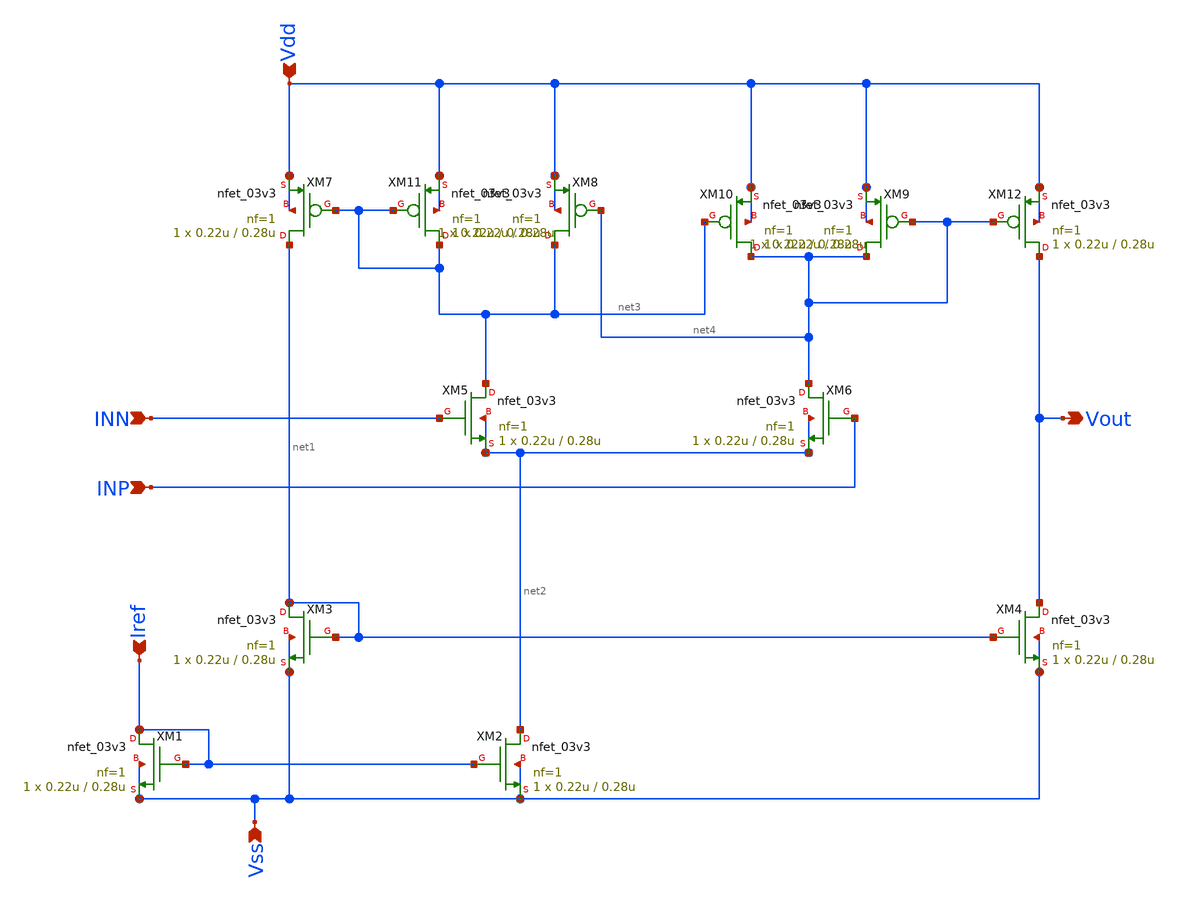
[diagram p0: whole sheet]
** sch_path: designs/libs/core_analog/Comparator/Comparator.sch
**.subckt Comparator Vss Vdd Iref INN INP Vout
*.ipin Vss
*.ipin Vdd
*.ipin Iref
*.ipin INN
*.ipin INP
*.opin Vout
XM1 Iref Iref Vss Vss nfet_03v3 L=0.28u W=0.22u nf=1 ad='int((nf+1)/2) * W/nf * 0.18u' as='int((nf+2)/2) * W/nf * 0.18u'
+ pd='2*int((nf+1)/2) * (W/nf + 0.18u)' ps='2*int((nf+2)/2) * (W/nf + 0.18u)' nrd='0.18u / W' nrs='0.18u / W'
+ sa=0 sb=0 sd=0 m=1
XM2 net2 Iref Vss Vss nfet_03v3 L=0.28u W=0.22u nf=1 ad='int((nf+1)/2) * W/nf * 0.18u' as='int((nf+2)/2) * W/nf * 0.18u'
+ pd='2*int((nf+1)/2) * (W/nf + 0.18u)' ps='2*int((nf+2)/2) * (W/nf + 0.18u)' nrd='0.18u / W' nrs='0.18u / W'
+ sa=0 sb=0 sd=0 m=1
XM3 net1 net1 Vss Vss nfet_03v3 L=0.28u W=0.22u nf=1 ad='int((nf+1)/2) * W/nf * 0.18u' as='int((nf+2)/2) * W/nf * 0.18u'
+ pd='2*int((nf+1)/2) * (W/nf + 0.18u)' ps='2*int((nf+2)/2) * (W/nf + 0.18u)' nrd='0.18u / W' nrs='0.18u / W'
+ sa=0 sb=0 sd=0 m=1
XM4 Vout net1 Vss Vss nfet_03v3 L=0.28u W=0.22u nf=1 ad='int((nf+1)/2) * W/nf * 0.18u' as='int((nf+2)/2) * W/nf * 0.18u'
+ pd='2*int((nf+1)/2) * (W/nf + 0.18u)' ps='2*int((nf+2)/2) * (W/nf + 0.18u)' nrd='0.18u / W' nrs='0.18u / W'
+ sa=0 sb=0 sd=0 m=1
XM5 net3 INN net2 net2 nfet_03v3 L=0.28u W=0.22u nf=1 ad='int((nf+1)/2) * W/nf * 0.18u' as='int((nf+2)/2) * W/nf * 0.18u'
+ pd='2*int((nf+1)/2) * (W/nf + 0.18u)' ps='2*int((nf+2)/2) * (W/nf + 0.18u)' nrd='0.18u / W' nrs='0.18u / W'
+ sa=0 sb=0 sd=0 m=1
XM6 net4 INP net2 net2 nfet_03v3 L=0.28u W=0.22u nf=1 ad='int((nf+1)/2) * W/nf * 0.18u' as='int((nf+2)/2) * W/nf * 0.18u'
+ pd='2*int((nf+1)/2) * (W/nf + 0.18u)' ps='2*int((nf+2)/2) * (W/nf + 0.18u)' nrd='0.18u / W' nrs='0.18u / W'
+ sa=0 sb=0 sd=0 m=1
XM7 net1 net3 Vdd Vdd nfet_03v3 L=0.28u W=0.22u nf=1 ad='int((nf+1)/2) * W/nf * 0.18u' as='int((nf+2)/2) * W/nf * 0.18u'
+ pd='2*int((nf+1)/2) * (W/nf + 0.18u)' ps='2*int((nf+2)/2) * (W/nf + 0.18u)' nrd='0.18u / W' nrs='0.18u / W'
+ sa=0 sb=0 sd=0 m=1
XM8 net3 net4 Vdd Vdd nfet_03v3 L=0.28u W=0.22u nf=1 ad='int((nf+1)/2) * W/nf * 0.18u' as='int((nf+2)/2) * W/nf * 0.18u'
+ pd='2*int((nf+1)/2) * (W/nf + 0.18u)' ps='2*int((nf+2)/2) * (W/nf + 0.18u)' nrd='0.18u / W' nrs='0.18u / W'
+ sa=0 sb=0 sd=0 m=1
XM9 net4 net4 Vdd Vdd nfet_03v3 L=0.28u W=0.22u nf=1 ad='int((nf+1)/2) * W/nf * 0.18u' as='int((nf+2)/2) * W/nf * 0.18u'
+ pd='2*int((nf+1)/2) * (W/nf + 0.18u)' ps='2*int((nf+2)/2) * (W/nf + 0.18u)' nrd='0.18u / W' nrs='0.18u / W'
+ sa=0 sb=0 sd=0 m=1
XM10 net4 net3 Vdd Vdd nfet_03v3 L=0.28u W=0.22u nf=1 ad='int((nf+1)/2) * W/nf * 0.18u' as='int((nf+2)/2) * W/nf * 0.18u'
+ pd='2*int((nf+1)/2) * (W/nf + 0.18u)' ps='2*int((nf+2)/2) * (W/nf + 0.18u)' nrd='0.18u / W' nrs='0.18u / W'
+ sa=0 sb=0 sd=0 m=1
XM11 net3 net3 Vdd Vdd nfet_03v3 L=0.28u W=0.22u nf=1 ad='int((nf+1)/2) * W/nf * 0.18u' as='int((nf+2)/2) * W/nf * 0.18u'
+ pd='2*int((nf+1)/2) * (W/nf + 0.18u)' ps='2*int((nf+2)/2) * (W/nf + 0.18u)' nrd='0.18u / W' nrs='0.18u / W'
+ sa=0 sb=0 sd=0 m=1
XM12 Vout net4 Vdd Vdd nfet_03v3 L=0.28u W=0.22u nf=1 ad='int((nf+1)/2) * W/nf * 0.18u' as='int((nf+2)/2) * W/nf * 0.18u'
+ pd='2*int((nf+1)/2) * (W/nf + 0.18u)' ps='2*int((nf+2)/2) * (W/nf + 0.18u)' nrd='0.18u / W' nrs='0.18u / W'
+ sa=0 sb=0 sd=0 m=1
**.ends
.end
